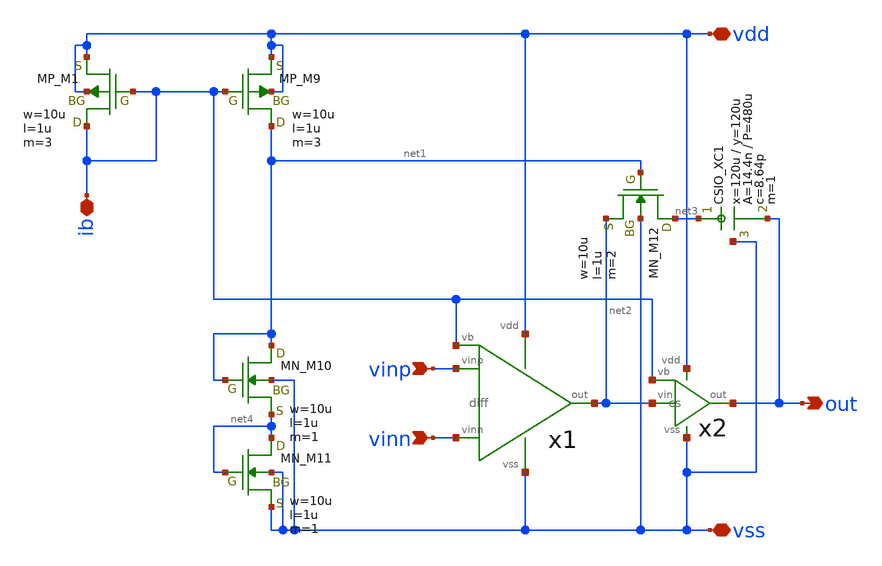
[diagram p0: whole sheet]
** sch_path: member_project/opamp/kubotakeshi/回路図/opamp_tk.sch
**.subckt opamp_tk vinp vinn out vdd vss ib
*.ipin vinp
*.ipin vinn
*.opin out
*.iopin vdd
*.iopin vss
*.iopin ib
x1 vinp vinn net2 vdd vss ib diff
x2 net2 ib out vdd vss cs
XM9 net1 ib vdd vdd PMOS w=10u l=1u as=0 ad=0 ps=0 pd=0 nrd=0 nrs=0 m=3
XM12 net3 net1 net2 vss NMOS w=10u l=1u as=0 ad=0 ps=0 pd=0 nrd=0 nrs=0 m=2
XM1 ib ib vdd vdd PMOS w=10u l=1u as=0 ad=0 ps=0 pd=0 nrd=0 nrs=0 m=3
XM10 net1 net1 net4 vss NMOS w=10u l=1u as=0 ad=0 ps=0 pd=0 nrd=0 nrs=0 m=1
XM11 net4 net4 vss vss NMOS w=10u l=1u as=0 ad=0 ps=0 pd=0 nrd=0 nrs=0 m=1
XXC1 net3 out vss F_CSIO c=8.64p x=120u y=120u m=1
**.ends

* expanding   symbol:  diff.sym # of pins=6
** sym_path: diff.sym
** sch_path: diff.sch
.subckt diff vinp vinn out vdd vss vb
*.ipin vinn
*.ipin vinp
*.ipin vb
*.opin out
*.iopin vdd
*.iopin vss
XM5 net2 vb vdd vdd PMOS w=10u l=1u as=0 ad=0 ps=0 pd=0 nrd=0 nrs=0 m=18
XM1 net1 vinn net2 net2 PMOS w=10u l=1u as=0 ad=0 ps=0 pd=0 nrd=0 nrs=0 m=36
XM2 out vinp net2 net2 PMOS w=10u l=1u as=0 ad=0 ps=0 pd=0 nrd=0 nrs=0 m=36
XM3 net1 net1 vss vss NMOS w=10u l=1u as=0 ad=0 ps=0 pd=0 nrd=0 nrs=0 m=3
XM4 out net1 vss vss NMOS w=10u l=1u as=0 ad=0 ps=0 pd=0 nrd=0 nrs=0 m=3
.ends


* expanding   symbol:  cs.sym # of pins=5
** sym_path: cs.sym
** sch_path: cs.sch
.subckt cs vin vb out vdd vss
*.ipin vb
*.ipin vin
*.opin out
*.iopin vss
*.iopin vdd
XM6 out vb vdd vdd PMOS w=10u l=1u as=0 ad=0 ps=0 pd=0 nrd=0 nrs=0 m=27
XM7 out vin vss vss NMOS w=10u l=1u as=0 ad=0 ps=0 pd=0 nrd=0 nrs=0 m=9
.ends

.end
